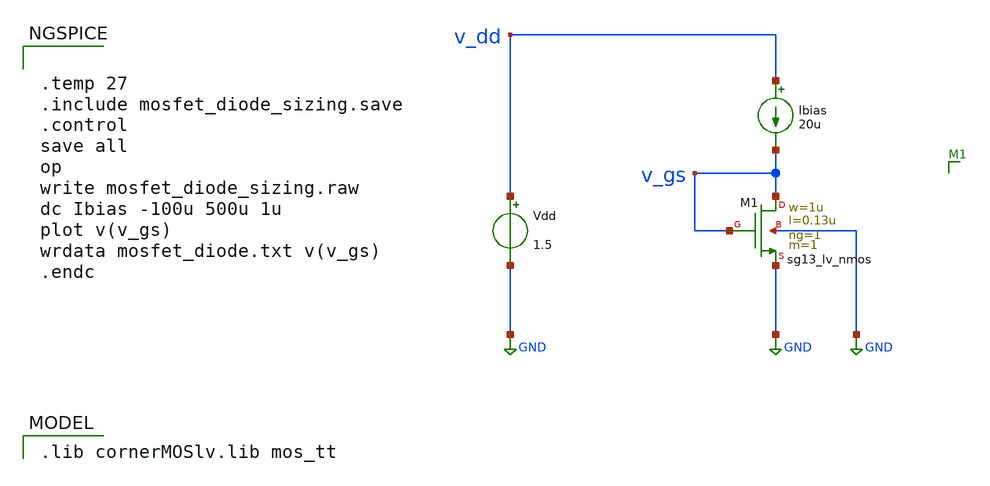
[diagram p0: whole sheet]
** sch_path: xschem/mosfet_diode_sizing.sch
* (c) 2024-2025 Harald Pretl, Apache-2.0 license
**.subckt mosfet_diode_sizing
Vdd v_dd GND 1.5
XM1 v_gs v_gs GND GND sg13_lv_nmos w=1u l=0.13u ng=1 m=1 mm_ok=1
Ibias v_dd v_gs 20u
**** begin user architecture code
 .lib cornerMOSlv.lib mos_tt



.temp 27
.include mosfet_diode_sizing.save
.control
save all
op
write mosfet_diode_sizing.raw
dc Ibias -100u 500u 1u
plot v(v_gs)
wrdata mosfet_diode.txt v(v_gs)
.endc


**** end user architecture code
**.ends
.GLOBAL GND
.end
